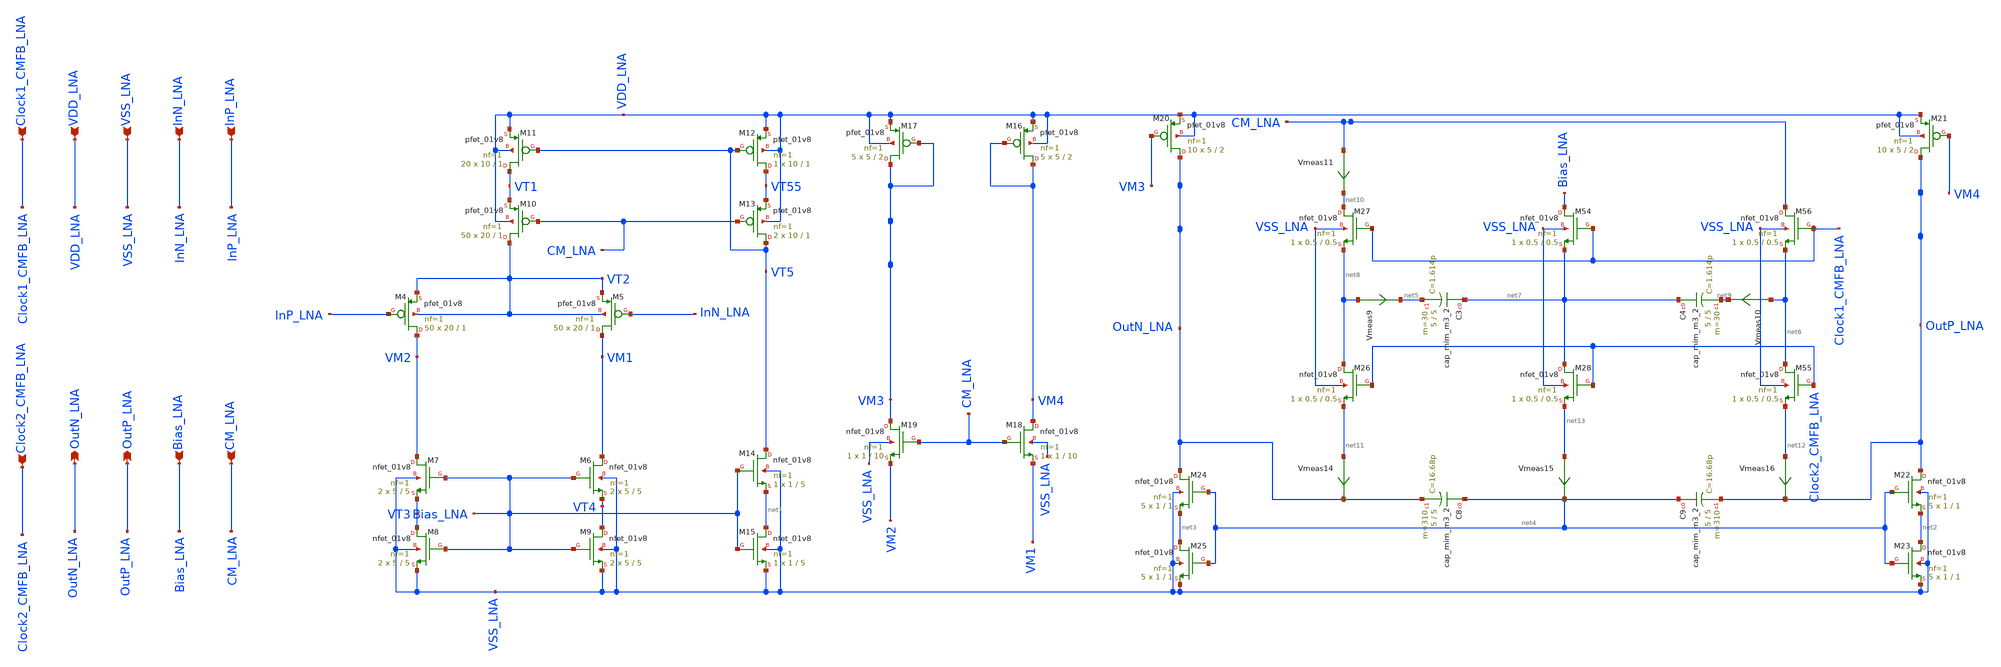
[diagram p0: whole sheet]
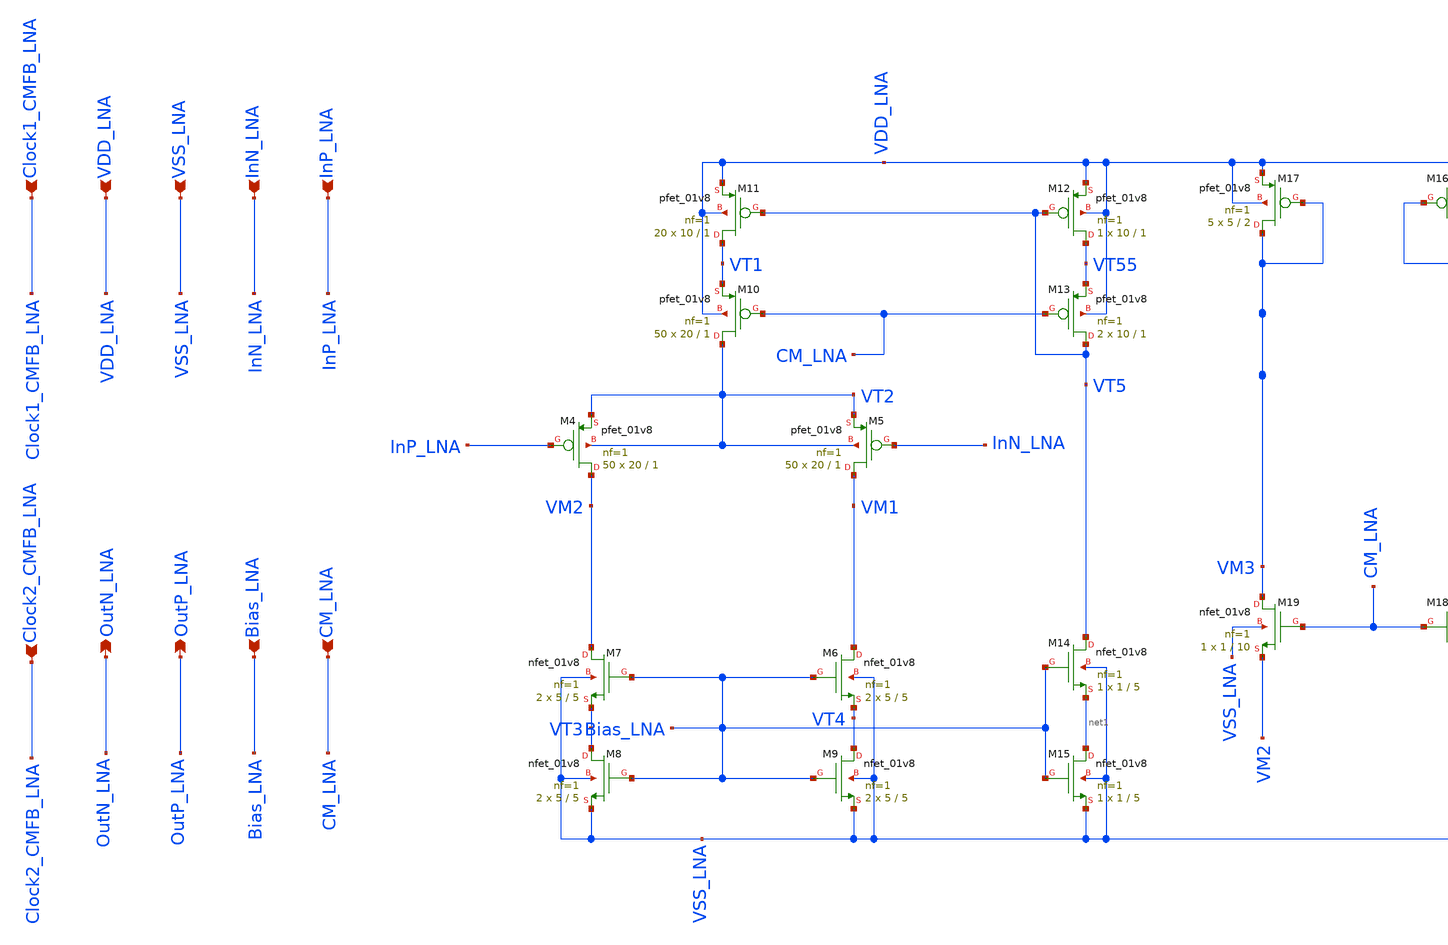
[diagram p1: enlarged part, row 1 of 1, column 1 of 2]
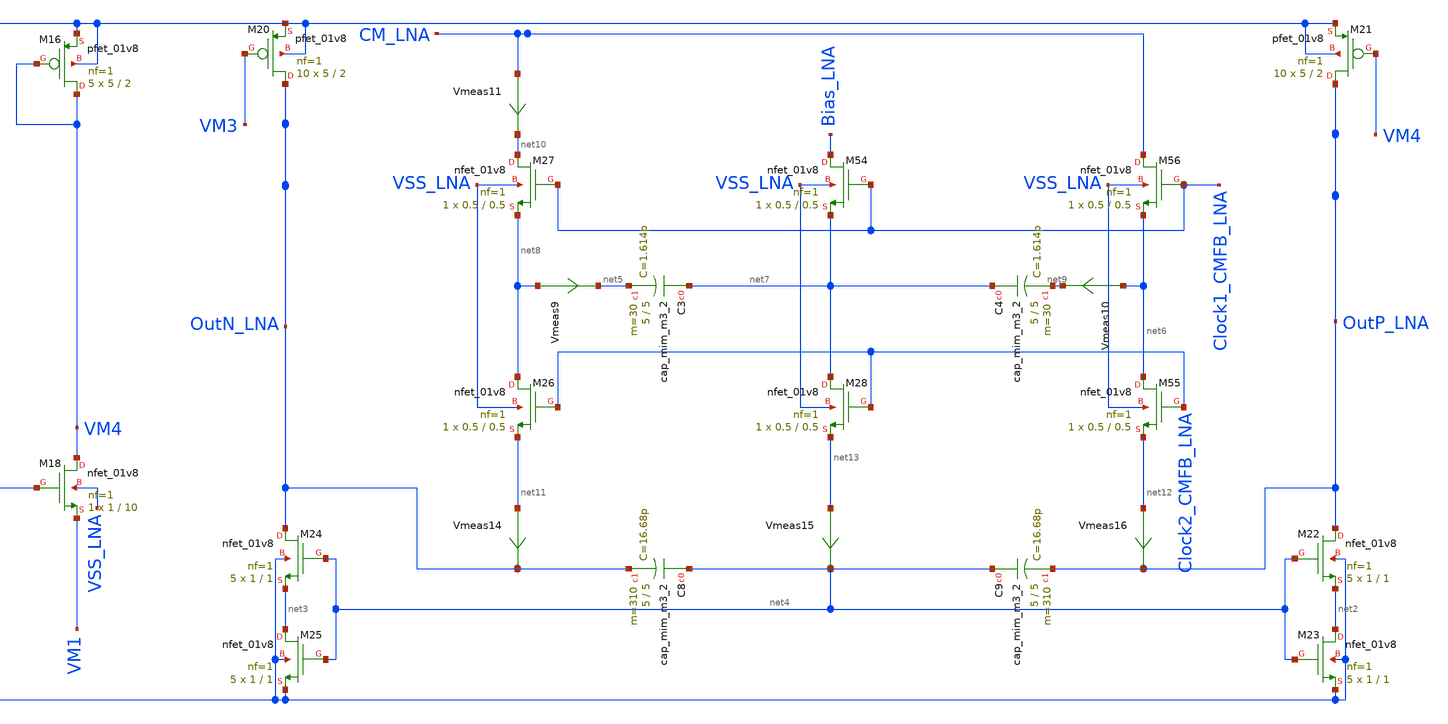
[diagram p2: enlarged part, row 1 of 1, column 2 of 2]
** sch_path: LNA_backup_tvt.sch
**.subckt LNA_backup_tvt InP_LNA InN_LNA VSS_LNA VDD_LNA CM_LNA Bias_LNA OutP_LNA OutN_LNA
*+ Clock1_CMFB_LNA Clock2_CMFB_LNA
*.ipin InP_LNA
*.ipin InN_LNA
*.ipin VSS_LNA
*.ipin VDD_LNA
*.ipin CM_LNA
*.ipin Bias_LNA
*.opin OutP_LNA
*.opin OutN_LNA
*.ipin Clock1_CMFB_LNA
*.ipin Clock2_CMFB_LNA
XM4 VM2 InP_LNA VT2 VT2 sky130_fd_pr__pfet_01v8 L=1 W=20 nf=1 ad='int((nf+1)/2) * W/nf * 0.29' as='int((nf+2)/2) * W/nf * 0.29'
+ pd='2*int((nf+1)/2) * (W/nf + 0.29)' ps='2*int((nf+2)/2) * (W/nf + 0.29)' nrd='0.29 / W' nrs='0.29 / W'
+ sa=0 sb=0 sd=0 mult=50 m=50
XM5 VM1 InN_LNA VT2 VT2 sky130_fd_pr__pfet_01v8 L=1 W=20 nf=1 ad='int((nf+1)/2) * W/nf * 0.29' as='int((nf+2)/2) * W/nf * 0.29'
+ pd='2*int((nf+1)/2) * (W/nf + 0.29)' ps='2*int((nf+2)/2) * (W/nf + 0.29)' nrd='0.29 / W' nrs='0.29 / W'
+ sa=0 sb=0 sd=0 mult=50 m=50
XM6 VM1 Bias_LNA VT4 VSS_LNA sky130_fd_pr__nfet_01v8 L=5 W=5 nf=1 ad='int((nf+1)/2) * W/nf * 0.29' as='int((nf+2)/2) * W/nf * 0.29'
+ pd='2*int((nf+1)/2) * (W/nf + 0.29)' ps='2*int((nf+2)/2) * (W/nf + 0.29)' nrd='0.29 / W' nrs='0.29 / W'
+ sa=0 sb=0 sd=0 mult=2 m=2
XM7 VM2 Bias_LNA VT3 VSS_LNA sky130_fd_pr__nfet_01v8 L=5 W=5 nf=1 ad='int((nf+1)/2) * W/nf * 0.29' as='int((nf+2)/2) * W/nf * 0.29'
+ pd='2*int((nf+1)/2) * (W/nf + 0.29)' ps='2*int((nf+2)/2) * (W/nf + 0.29)' nrd='0.29 / W' nrs='0.29 / W'
+ sa=0 sb=0 sd=0 mult=2 m=2
XM8 VT3 Bias_LNA VSS_LNA VSS_LNA sky130_fd_pr__nfet_01v8 L=5 W=5 nf=1 ad='int((nf+1)/2) * W/nf * 0.29'
+ as='int((nf+2)/2) * W/nf * 0.29' pd='2*int((nf+1)/2) * (W/nf + 0.29)' ps='2*int((nf+2)/2) * (W/nf + 0.29)'
+ nrd='0.29 / W' nrs='0.29 / W' sa=0 sb=0 sd=0 mult=2 m=2
XM9 VT4 Bias_LNA VSS_LNA VSS_LNA sky130_fd_pr__nfet_01v8 L=5 W=5 nf=1 ad='int((nf+1)/2) * W/nf * 0.29'
+ as='int((nf+2)/2) * W/nf * 0.29' pd='2*int((nf+1)/2) * (W/nf + 0.29)' ps='2*int((nf+2)/2) * (W/nf + 0.29)'
+ nrd='0.29 / W' nrs='0.29 / W' sa=0 sb=0 sd=0 mult=2 m=2
XM10 VT2 CM_LNA VT1 VDD_LNA sky130_fd_pr__pfet_01v8 L=1 W=20 nf=1 ad='int((nf+1)/2) * W/nf * 0.29' as='int((nf+2)/2) * W/nf * 0.29'
+ pd='2*int((nf+1)/2) * (W/nf + 0.29)' ps='2*int((nf+2)/2) * (W/nf + 0.29)' nrd='0.29 / W' nrs='0.29 / W'
+ sa=0 sb=0 sd=0 mult=50 m=50
XM11 VT1 VT5 VDD_LNA VDD_LNA sky130_fd_pr__pfet_01v8 L=1 W=10 nf=1 ad='int((nf+1)/2) * W/nf * 0.29' as='int((nf+2)/2) * W/nf * 0.29'
+ pd='2*int((nf+1)/2) * (W/nf + 0.29)' ps='2*int((nf+2)/2) * (W/nf + 0.29)' nrd='0.29 / W' nrs='0.29 / W'
+ sa=0 sb=0 sd=0 mult=20 m=20
XM12 VT55 VT5 VDD_LNA VDD_LNA sky130_fd_pr__pfet_01v8 L=1 W=10 nf=1 ad='int((nf+1)/2) * W/nf * 0.29'
+ as='int((nf+2)/2) * W/nf * 0.29' pd='2*int((nf+1)/2) * (W/nf + 0.29)' ps='2*int((nf+2)/2) * (W/nf + 0.29)'
+ nrd='0.29 / W' nrs='0.29 / W' sa=0 sb=0 sd=0 mult=1 m=1
XM13 VT5 CM_LNA VT55 VDD_LNA sky130_fd_pr__pfet_01v8 L=1 W=10 nf=1 ad='int((nf+1)/2) * W/nf * 0.29' as='int((nf+2)/2) * W/nf * 0.29'
+ pd='2*int((nf+1)/2) * (W/nf + 0.29)' ps='2*int((nf+2)/2) * (W/nf + 0.29)' nrd='0.29 / W' nrs='0.29 / W'
+ sa=0 sb=0 sd=0 mult=2 m=2
XM14 VT5 Bias_LNA net1 VSS_LNA sky130_fd_pr__nfet_01v8 L=5 W=1 nf=1 ad='int((nf+1)/2) * W/nf * 0.29'
+ as='int((nf+2)/2) * W/nf * 0.29' pd='2*int((nf+1)/2) * (W/nf + 0.29)' ps='2*int((nf+2)/2) * (W/nf + 0.29)'
+ nrd='0.29 / W' nrs='0.29 / W' sa=0 sb=0 sd=0 mult=1 m=1
XM15 net1 Bias_LNA VSS_LNA VSS_LNA sky130_fd_pr__nfet_01v8 L=5 W=1 nf=1 ad='int((nf+1)/2) * W/nf * 0.29'
+ as='int((nf+2)/2) * W/nf * 0.29' pd='2*int((nf+1)/2) * (W/nf + 0.29)' ps='2*int((nf+2)/2) * (W/nf + 0.29)'
+ nrd='0.29 / W' nrs='0.29 / W' sa=0 sb=0 sd=0 mult=1 m=1
XM16 VM4 VM4 VDD_LNA VDD_LNA sky130_fd_pr__pfet_01v8 L=2 W=5 nf=1 ad='int((nf+1)/2) * W/nf * 0.29' as='int((nf+2)/2) * W/nf * 0.29'
+ pd='2*int((nf+1)/2) * (W/nf + 0.29)' ps='2*int((nf+2)/2) * (W/nf + 0.29)' nrd='0.29 / W' nrs='0.29 / W'
+ sa=0 sb=0 sd=0 mult=5 m=5
XM17 VM3 VM3 VDD_LNA VDD_LNA sky130_fd_pr__pfet_01v8 L=2 W=5 nf=1 ad='int((nf+1)/2) * W/nf * 0.29' as='int((nf+2)/2) * W/nf * 0.29'
+ pd='2*int((nf+1)/2) * (W/nf + 0.29)' ps='2*int((nf+2)/2) * (W/nf + 0.29)' nrd='0.29 / W' nrs='0.29 / W'
+ sa=0 sb=0 sd=0 mult=5 m=5
XM18 VM4 CM_LNA VM1 VSS_LNA sky130_fd_pr__nfet_01v8 L=10 W=1 nf=1 ad='int((nf+1)/2) * W/nf * 0.29' as='int((nf+2)/2) * W/nf * 0.29'
+ pd='2*int((nf+1)/2) * (W/nf + 0.29)' ps='2*int((nf+2)/2) * (W/nf + 0.29)' nrd='0.29 / W' nrs='0.29 / W'
+ sa=0 sb=0 sd=0 mult=1 m=1
XM19 VM3 CM_LNA VM2 VSS_LNA sky130_fd_pr__nfet_01v8 L=10 W=1 nf=1 ad='int((nf+1)/2) * W/nf * 0.29' as='int((nf+2)/2) * W/nf * 0.29'
+ pd='2*int((nf+1)/2) * (W/nf + 0.29)' ps='2*int((nf+2)/2) * (W/nf + 0.29)' nrd='0.29 / W' nrs='0.29 / W'
+ sa=0 sb=0 sd=0 mult=1 m=1
XM20 OutN_LNA VM3 VDD_LNA VDD_LNA sky130_fd_pr__pfet_01v8 L=2 W=5 nf=1 ad='int((nf+1)/2) * W/nf * 0.29'
+ as='int((nf+2)/2) * W/nf * 0.29' pd='2*int((nf+1)/2) * (W/nf + 0.29)' ps='2*int((nf+2)/2) * (W/nf + 0.29)'
+ nrd='0.29 / W' nrs='0.29 / W' sa=0 sb=0 sd=0 mult=10 m=10
XM21 OutP_LNA VM4 VDD_LNA VDD_LNA sky130_fd_pr__pfet_01v8 L=2 W=5 nf=1 ad='int((nf+1)/2) * W/nf * 0.29'
+ as='int((nf+2)/2) * W/nf * 0.29' pd='2*int((nf+1)/2) * (W/nf + 0.29)' ps='2*int((nf+2)/2) * (W/nf + 0.29)'
+ nrd='0.29 / W' nrs='0.29 / W' sa=0 sb=0 sd=0 mult=10 m=10
XM22 OutP_LNA net4 net2 VSS_LNA sky130_fd_pr__nfet_01v8 L=1 W=1 nf=1 ad='int((nf+1)/2) * W/nf * 0.29'
+ as='int((nf+2)/2) * W/nf * 0.29' pd='2*int((nf+1)/2) * (W/nf + 0.29)' ps='2*int((nf+2)/2) * (W/nf + 0.29)'
+ nrd='0.29 / W' nrs='0.29 / W' sa=0 sb=0 sd=0 mult=5 m=5
XM23 net2 net4 VSS_LNA VSS_LNA sky130_fd_pr__nfet_01v8 L=1 W=1 nf=1 ad='int((nf+1)/2) * W/nf * 0.29'
+ as='int((nf+2)/2) * W/nf * 0.29' pd='2*int((nf+1)/2) * (W/nf + 0.29)' ps='2*int((nf+2)/2) * (W/nf + 0.29)'
+ nrd='0.29 / W' nrs='0.29 / W' sa=0 sb=0 sd=0 mult=5 m=5
XM24 OutN_LNA net4 net3 VSS_LNA sky130_fd_pr__nfet_01v8 L=1 W=1 nf=1 ad='int((nf+1)/2) * W/nf * 0.29'
+ as='int((nf+2)/2) * W/nf * 0.29' pd='2*int((nf+1)/2) * (W/nf + 0.29)' ps='2*int((nf+2)/2) * (W/nf + 0.29)'
+ nrd='0.29 / W' nrs='0.29 / W' sa=0 sb=0 sd=0 mult=5 m=5
XM25 net3 net4 VSS_LNA VSS_LNA sky130_fd_pr__nfet_01v8 L=1 W=1 nf=1 ad='int((nf+1)/2) * W/nf * 0.29'
+ as='int((nf+2)/2) * W/nf * 0.29' pd='2*int((nf+1)/2) * (W/nf + 0.29)' ps='2*int((nf+2)/2) * (W/nf + 0.29)'
+ nrd='0.29 / W' nrs='0.29 / W' sa=0 sb=0 sd=0 mult=5 m=5
XC3 net7 net5 sky130_fd_pr__cap_mim_m3_2 W=5 L=5 MF=30 m=30
XC4 net7 net9 sky130_fd_pr__cap_mim_m3_2 W=5 L=5 MF=30 m=30
XC8 net4 OutN_LNA sky130_fd_pr__cap_mim_m3_2 W=5 L=5 MF=310 m=310
XC9 net4 OutP_LNA sky130_fd_pr__cap_mim_m3_2 W=5 L=5 MF=310 m=310
XM26 net8 Clock2_CMFB_LNA net11 VSS_LNA sky130_fd_pr__nfet_01v8 L=0.5 W=0.5 nf=1 ad='int((nf+1)/2) * W/nf * 0.29'
+ as='int((nf+2)/2) * W/nf * 0.29' pd='2*int((nf+1)/2) * (W/nf + 0.29)' ps='2*int((nf+2)/2) * (W/nf + 0.29)'
+ nrd='0.29 / W' nrs='0.29 / W' sa=0 sb=0 sd=0 mult=1 m=1
XM27 net10 Clock1_CMFB_LNA net8 VSS_LNA sky130_fd_pr__nfet_01v8 L=0.5 W=0.5 nf=1 ad='int((nf+1)/2) * W/nf * 0.29'
+ as='int((nf+2)/2) * W/nf * 0.29' pd='2*int((nf+1)/2) * (W/nf + 0.29)' ps='2*int((nf+2)/2) * (W/nf + 0.29)'
+ nrd='0.29 / W' nrs='0.29 / W' sa=0 sb=0 sd=0 mult=1 m=1
XM28 net7 Clock2_CMFB_LNA net13 VSS_LNA sky130_fd_pr__nfet_01v8 L=0.5 W=0.5 nf=1 ad='int((nf+1)/2) * W/nf * 0.29'
+ as='int((nf+2)/2) * W/nf * 0.29' pd='2*int((nf+1)/2) * (W/nf + 0.29)' ps='2*int((nf+2)/2) * (W/nf + 0.29)'
+ nrd='0.29 / W' nrs='0.29 / W' sa=0 sb=0 sd=0 mult=1 m=1
XM54 Bias_LNA Clock1_CMFB_LNA net7 VSS_LNA sky130_fd_pr__nfet_01v8 L=0.5 W=0.5 nf=1 ad='int((nf+1)/2) * W/nf * 0.29'
+ as='int((nf+2)/2) * W/nf * 0.29' pd='2*int((nf+1)/2) * (W/nf + 0.29)' ps='2*int((nf+2)/2) * (W/nf + 0.29)'
+ nrd='0.29 / W' nrs='0.29 / W' sa=0 sb=0 sd=0 mult=1 m=1
XM55 net6 Clock2_CMFB_LNA net12 VSS_LNA sky130_fd_pr__nfet_01v8 L=0.5 W=0.5 nf=1 ad='int((nf+1)/2) * W/nf * 0.29'
+ as='int((nf+2)/2) * W/nf * 0.29' pd='2*int((nf+1)/2) * (W/nf + 0.29)' ps='2*int((nf+2)/2) * (W/nf + 0.29)'
+ nrd='0.29 / W' nrs='0.29 / W' sa=0 sb=0 sd=0 mult=1 m=1
XM56 CM_LNA Clock1_CMFB_LNA net6 VSS_LNA sky130_fd_pr__nfet_01v8 L=0.5 W=0.5 nf=1 ad='int((nf+1)/2) * W/nf * 0.29'
+ as='int((nf+2)/2) * W/nf * 0.29' pd='2*int((nf+1)/2) * (W/nf + 0.29)' ps='2*int((nf+2)/2) * (W/nf + 0.29)'
+ nrd='0.29 / W' nrs='0.29 / W' sa=0 sb=0 sd=0 mult=1 m=1
Vmeas9 net8 net5 0
.save i(vmeas9)
Vmeas10 net6 net9 0
.save i(vmeas10)
Vmeas11 CM_LNA net10 0
.save i(vmeas11)
Vmeas14 net11 OutN_LNA 0
.save i(vmeas14)
Vmeas15 net13 net4 0
.save i(vmeas15)
Vmeas16 net12 OutP_LNA 0
.save i(vmeas16)
**.ends
.end
